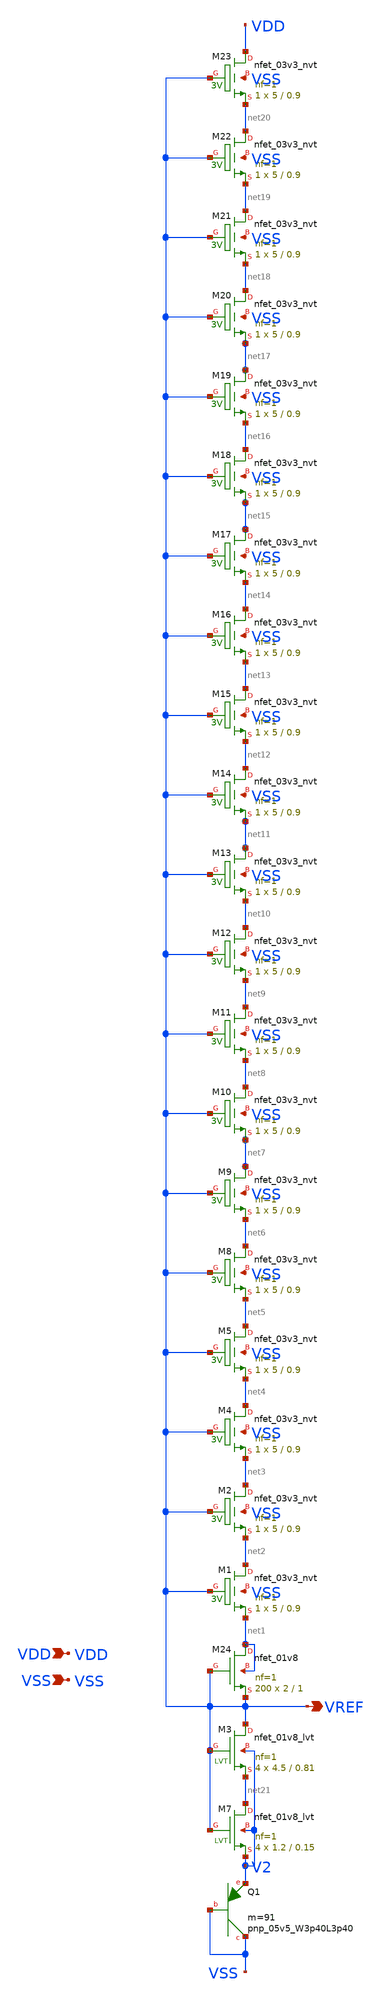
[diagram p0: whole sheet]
** sch_path: design/LELO_SVOD_SKY130A/LELO_SVOD_VTREF.sch
**.subckt LELO_SVOD_VTREF VDD VSS VREF
*.ipin VDD
*.ipin VSS
*.opin VREF
XM1 net2 VREF net1 VSS sky130_fd_pr__nfet_03v3_nvt L=0.9 W=5 nf=1 ad='int((1 + 1)/2) * 5 / 1 * 0.29'
+ as='int((1 + 2)/2) * 5 / 1 * 0.29' pd='2*int((1 + 1)/2) * (5 / 1 + 0.29)' ps='2*int((1 + 2)/2) * (5 / 1 + 0.29)'
+ nrd='0.29 / 5 ' nrs='0.29 / 5 ' sa=0 sb=0 sd=0 mult=1 m=1
XM2 net3 VREF net2 VSS sky130_fd_pr__nfet_03v3_nvt L=0.9 W=5 nf=1 ad='int((1 + 1)/2) * 5 / 1 * 0.29'
+ as='int((1 + 2)/2) * 5 / 1 * 0.29' pd='2*int((1 + 1)/2) * (5 / 1 + 0.29)' ps='2*int((1 + 2)/2) * (5 / 1 + 0.29)'
+ nrd='0.29 / 5 ' nrs='0.29 / 5 ' sa=0 sb=0 sd=0 mult=1 m=1
XM4 net4 VREF net3 VSS sky130_fd_pr__nfet_03v3_nvt L=0.9 W=5 nf=1 ad='int((1 + 1)/2) * 5 / 1 * 0.29'
+ as='int((1 + 2)/2) * 5 / 1 * 0.29' pd='2*int((1 + 1)/2) * (5 / 1 + 0.29)' ps='2*int((1 + 2)/2) * (5 / 1 + 0.29)'
+ nrd='0.29 / 5 ' nrs='0.29 / 5 ' sa=0 sb=0 sd=0 mult=1 m=1
XM5 net5 VREF net4 VSS sky130_fd_pr__nfet_03v3_nvt L=0.9 W=5 nf=1 ad='int((1 + 1)/2) * 5 / 1 * 0.29'
+ as='int((1 + 2)/2) * 5 / 1 * 0.29' pd='2*int((1 + 1)/2) * (5 / 1 + 0.29)' ps='2*int((1 + 2)/2) * (5 / 1 + 0.29)'
+ nrd='0.29 / 5 ' nrs='0.29 / 5 ' sa=0 sb=0 sd=0 mult=1 m=1
XM8 net6 VREF net5 VSS sky130_fd_pr__nfet_03v3_nvt L=0.9 W=5 nf=1 ad='int((1 + 1)/2) * 5 / 1 * 0.29'
+ as='int((1 + 2)/2) * 5 / 1 * 0.29' pd='2*int((1 + 1)/2) * (5 / 1 + 0.29)' ps='2*int((1 + 2)/2) * (5 / 1 + 0.29)'
+ nrd='0.29 / 5 ' nrs='0.29 / 5 ' sa=0 sb=0 sd=0 mult=1 m=1
XM9 net7 VREF net6 VSS sky130_fd_pr__nfet_03v3_nvt L=0.9 W=5 nf=1 ad='int((1 + 1)/2) * 5 / 1 * 0.29'
+ as='int((1 + 2)/2) * 5 / 1 * 0.29' pd='2*int((1 + 1)/2) * (5 / 1 + 0.29)' ps='2*int((1 + 2)/2) * (5 / 1 + 0.29)'
+ nrd='0.29 / 5 ' nrs='0.29 / 5 ' sa=0 sb=0 sd=0 mult=1 m=1
XM10 net8 VREF net7 VSS sky130_fd_pr__nfet_03v3_nvt L=0.9 W=5 nf=1 ad='int((1 + 1)/2) * 5 / 1 * 0.29'
+ as='int((1 + 2)/2) * 5 / 1 * 0.29' pd='2*int((1 + 1)/2) * (5 / 1 + 0.29)' ps='2*int((1 + 2)/2) * (5 / 1 + 0.29)'
+ nrd='0.29 / 5 ' nrs='0.29 / 5 ' sa=0 sb=0 sd=0 mult=1 m=1
XM11 net9 VREF net8 VSS sky130_fd_pr__nfet_03v3_nvt L=0.9 W=5 nf=1 ad='int((1 + 1)/2) * 5 / 1 * 0.29'
+ as='int((1 + 2)/2) * 5 / 1 * 0.29' pd='2*int((1 + 1)/2) * (5 / 1 + 0.29)' ps='2*int((1 + 2)/2) * (5 / 1 + 0.29)'
+ nrd='0.29 / 5 ' nrs='0.29 / 5 ' sa=0 sb=0 sd=0 mult=1 m=1
XM12 net10 VREF net9 VSS sky130_fd_pr__nfet_03v3_nvt L=0.9 W=5 nf=1 ad='int((1 + 1)/2) * 5 / 1 * 0.29'
+ as='int((1 + 2)/2) * 5 / 1 * 0.29' pd='2*int((1 + 1)/2) * (5 / 1 + 0.29)' ps='2*int((1 + 2)/2) * (5 / 1 + 0.29)'
+ nrd='0.29 / 5 ' nrs='0.29 / 5 ' sa=0 sb=0 sd=0 mult=1 m=1
XM13 net11 VREF net10 VSS sky130_fd_pr__nfet_03v3_nvt L=0.9 W=5 nf=1 ad='int((1 + 1)/2) * 5 / 1 * 0.29'
+ as='int((1 + 2)/2) * 5 / 1 * 0.29' pd='2*int((1 + 1)/2) * (5 / 1 + 0.29)' ps='2*int((1 + 2)/2) * (5 / 1 + 0.29)'
+ nrd='0.29 / 5 ' nrs='0.29 / 5 ' sa=0 sb=0 sd=0 mult=1 m=1
XM14 net12 VREF net11 VSS sky130_fd_pr__nfet_03v3_nvt L=0.9 W=5 nf=1 ad='int((1 + 1)/2) * 5 / 1 * 0.29'
+ as='int((1 + 2)/2) * 5 / 1 * 0.29' pd='2*int((1 + 1)/2) * (5 / 1 + 0.29)' ps='2*int((1 + 2)/2) * (5 / 1 + 0.29)'
+ nrd='0.29 / 5 ' nrs='0.29 / 5 ' sa=0 sb=0 sd=0 mult=1 m=1
XM15 net13 VREF net12 VSS sky130_fd_pr__nfet_03v3_nvt L=0.9 W=5 nf=1 ad='int((1 + 1)/2) * 5 / 1 * 0.29'
+ as='int((1 + 2)/2) * 5 / 1 * 0.29' pd='2*int((1 + 1)/2) * (5 / 1 + 0.29)' ps='2*int((1 + 2)/2) * (5 / 1 + 0.29)'
+ nrd='0.29 / 5 ' nrs='0.29 / 5 ' sa=0 sb=0 sd=0 mult=1 m=1
XM16 net14 VREF net13 VSS sky130_fd_pr__nfet_03v3_nvt L=0.9 W=5 nf=1 ad='int((1 + 1)/2) * 5 / 1 * 0.29'
+ as='int((1 + 2)/2) * 5 / 1 * 0.29' pd='2*int((1 + 1)/2) * (5 / 1 + 0.29)' ps='2*int((1 + 2)/2) * (5 / 1 + 0.29)'
+ nrd='0.29 / 5 ' nrs='0.29 / 5 ' sa=0 sb=0 sd=0 mult=1 m=1
XM17 net15 VREF net14 VSS sky130_fd_pr__nfet_03v3_nvt L=0.9 W=5 nf=1 ad='int((1 + 1)/2) * 5 / 1 * 0.29'
+ as='int((1 + 2)/2) * 5 / 1 * 0.29' pd='2*int((1 + 1)/2) * (5 / 1 + 0.29)' ps='2*int((1 + 2)/2) * (5 / 1 + 0.29)'
+ nrd='0.29 / 5 ' nrs='0.29 / 5 ' sa=0 sb=0 sd=0 mult=1 m=1
XM18 net16 VREF net15 VSS sky130_fd_pr__nfet_03v3_nvt L=0.9 W=5 nf=1 ad='int((1 + 1)/2) * 5 / 1 * 0.29'
+ as='int((1 + 2)/2) * 5 / 1 * 0.29' pd='2*int((1 + 1)/2) * (5 / 1 + 0.29)' ps='2*int((1 + 2)/2) * (5 / 1 + 0.29)'
+ nrd='0.29 / 5 ' nrs='0.29 / 5 ' sa=0 sb=0 sd=0 mult=1 m=1
XM19 net17 VREF net16 VSS sky130_fd_pr__nfet_03v3_nvt L=0.9 W=5 nf=1 ad='int((1 + 1)/2) * 5 / 1 * 0.29'
+ as='int((1 + 2)/2) * 5 / 1 * 0.29' pd='2*int((1 + 1)/2) * (5 / 1 + 0.29)' ps='2*int((1 + 2)/2) * (5 / 1 + 0.29)'
+ nrd='0.29 / 5 ' nrs='0.29 / 5 ' sa=0 sb=0 sd=0 mult=1 m=1
XM20 net18 VREF net17 VSS sky130_fd_pr__nfet_03v3_nvt L=0.9 W=5 nf=1 ad='int((1 + 1)/2) * 5 / 1 * 0.29'
+ as='int((1 + 2)/2) * 5 / 1 * 0.29' pd='2*int((1 + 1)/2) * (5 / 1 + 0.29)' ps='2*int((1 + 2)/2) * (5 / 1 + 0.29)'
+ nrd='0.29 / 5 ' nrs='0.29 / 5 ' sa=0 sb=0 sd=0 mult=1 m=1
XM21 net19 VREF net18 VSS sky130_fd_pr__nfet_03v3_nvt L=0.9 W=5 nf=1 ad='int((1 + 1)/2) * 5 / 1 * 0.29'
+ as='int((1 + 2)/2) * 5 / 1 * 0.29' pd='2*int((1 + 1)/2) * (5 / 1 + 0.29)' ps='2*int((1 + 2)/2) * (5 / 1 + 0.29)'
+ nrd='0.29 / 5 ' nrs='0.29 / 5 ' sa=0 sb=0 sd=0 mult=1 m=1
XM22 net20 VREF net19 VSS sky130_fd_pr__nfet_03v3_nvt L=0.9 W=5 nf=1 ad='int((1 + 1)/2) * 5 / 1 * 0.29'
+ as='int((1 + 2)/2) * 5 / 1 * 0.29' pd='2*int((1 + 1)/2) * (5 / 1 + 0.29)' ps='2*int((1 + 2)/2) * (5 / 1 + 0.29)'
+ nrd='0.29 / 5 ' nrs='0.29 / 5 ' sa=0 sb=0 sd=0 mult=1 m=1
XM23 VDD VREF net20 VSS sky130_fd_pr__nfet_03v3_nvt L=0.9 W=5 nf=1 ad='int((1 + 1)/2) * 5 / 1 * 0.29'
+ as='int((1 + 2)/2) * 5 / 1 * 0.29' pd='2*int((1 + 1)/2) * (5 / 1 + 0.29)' ps='2*int((1 + 2)/2) * (5 / 1 + 0.29)'
+ nrd='0.29 / 5 ' nrs='0.29 / 5 ' sa=0 sb=0 sd=0 mult=1 m=1
XQ1 VSS VSS V2 sky130_fd_pr__pnp_05v5_W3p40L3p40 m=91
XM3 VREF VREF net21 V2 sky130_fd_pr__nfet_01v8_lvt L=0.81 W=4.5 nf=1 ad='int((1 + 1)/2) * 4.5 / 1 * 0.29'
+ as='int((1 + 2)/2) * 4.5 / 1 * 0.29' pd='2*int((1 + 1)/2) * (4.5 / 1 + 0.29)' ps='2*int((1 + 2)/2) * (4.5 / 1 + 0.29)'
+ nrd='0.29 / 4.5 ' nrs='0.29 / 4.5 ' sa=0 sb=0 sd=0 mult=4 m=4
XM7 net21 VREF V2 V2 sky130_fd_pr__nfet_01v8_lvt L=0.15 W=1.2 nf=1 ad='int((1 + 1)/2) * 1.2 / 1 * 0.29'
+ as='int((1 + 2)/2) * 1.2 / 1 * 0.29' pd='2*int((1 + 1)/2) * (1.2 / 1 + 0.29)' ps='2*int((1 + 2)/2) * (1.2 / 1 + 0.29)'
+ nrd='0.29 / 1.2 ' nrs='0.29 / 1.2 ' sa=0 sb=0 sd=0 mult=4 m=4
XM24 net1 VREF VREF net1 sky130_fd_pr__nfet_01v8 L=1 W=2 nf=1 ad='int((1 + 1)/2) * 2 / 1 * 0.29' as='int((1 + 2)/2) * 2 / 1 * 0.29'
+ pd='2*int((1 + 1)/2) * (2 / 1 + 0.29)' ps='2*int((1 + 2)/2) * (2 / 1 + 0.29)' nrd='0.29 / 2 ' nrs='0.29 / 2 '
+ sa=0 sb=0 sd=0 mult=200 m=200
**.ends
.end
